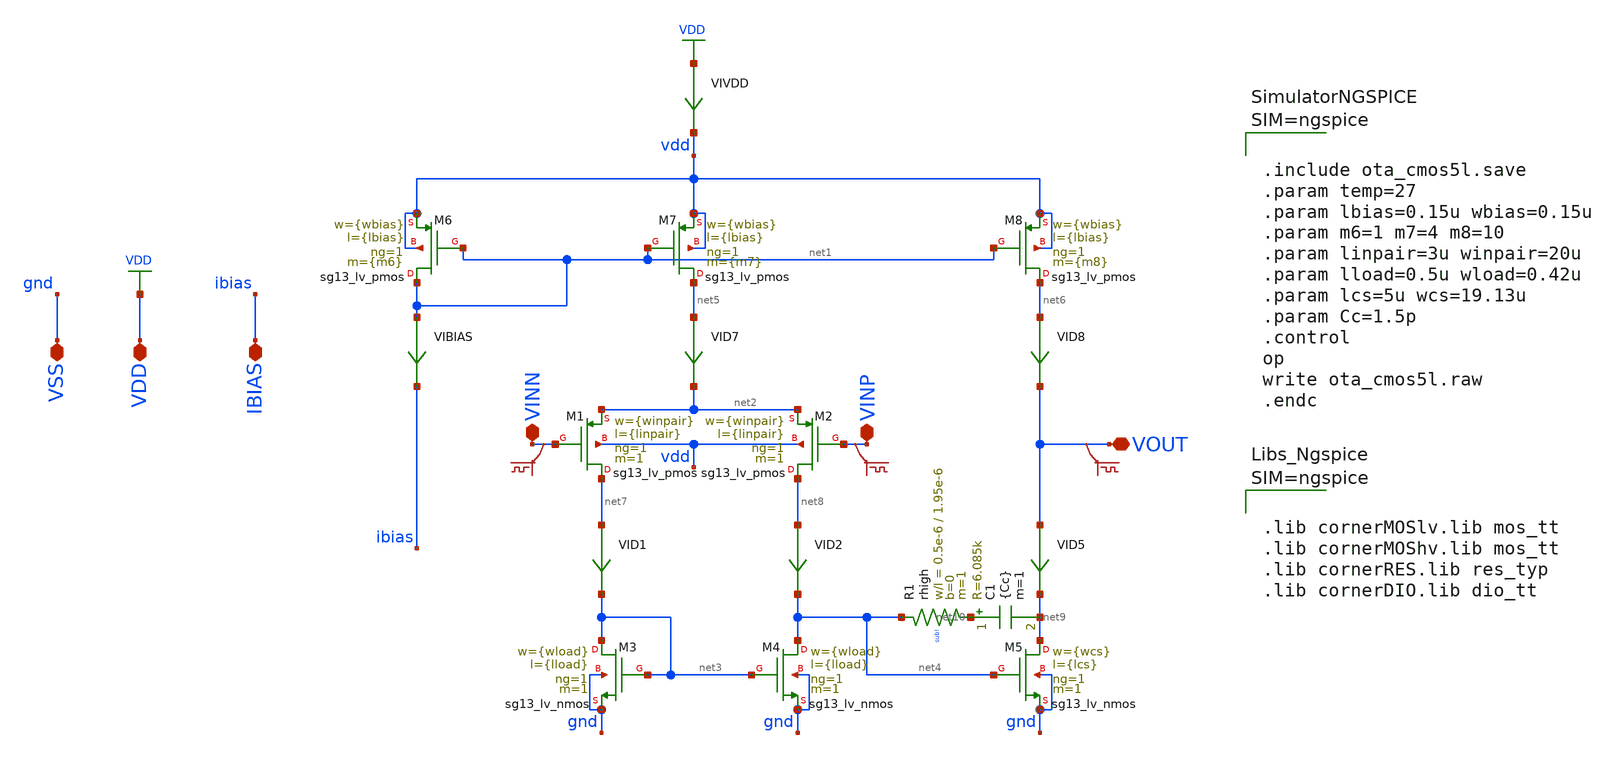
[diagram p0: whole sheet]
** sch_path: designs/libs/core_analog/ota_cmos5l/ota_cmos5l.sch
**.subckt ota_cmos5l IBIAS VDD VSS VOUT VINP VINN
*.iopin IBIAS
*.iopin VDD
*.iopin VSS
*.iopin VOUT
*.iopin VINP
*.iopin VINN
XM6 net1 net1 vdd vdd sg13_lv_pmos w={wbias} l={lbias} ng=1 m={m6} mm_ok=1
XM7 net5 net1 vdd vdd sg13_lv_pmos w={wbias} l={lbias} ng=1 m={m7} mm_ok=1
XM8 net6 net1 vdd vdd sg13_lv_pmos w={wbias} l={lbias} ng=1 m={m8} mm_ok=1
XM1 net7 VINN net2 vdd sg13_lv_pmos w={winpair} l={linpair} ng=1 m=1 mm_ok=1
XM2 net8 VINP net2 vdd sg13_lv_pmos w={winpair} l={linpair} ng=1 m=1 mm_ok=1
XM3 net3 net3 gnd gnd sg13_lv_nmos w={wload} l={lload} ng=1 m=1 mm_ok=1
XM4 net4 net3 gnd gnd sg13_lv_nmos w={wload} l={lload} ng=1 m=1 mm_ok=1
XM5 net9 net4 gnd gnd sg13_lv_nmos w={wcs} l={lcs} ng=1 m=1 mm_ok=1
C1 net10 net9 {Cc} m=1
XR1 net4 net10 sub! rhigh w=0.5e-6 l=1.95e-6 m=1 b=0 mm_ok=1
VIBIAS net1 ibias 0
.save i(vibias)
VID7 net5 net2 0
.save i(vid7)
VID8 net6 VOUT 0
.save i(vid8)
VIVDD VDD vdd 0
.save i(vivdd)
.save v(vinp)
.save v(vinn)
.save v(vout)
VID1 net7 net3 0
.save i(vid1)
VID2 net8 net4 0
.save i(vid2)
VID5 VOUT net9 0
.save i(vid5)
**** begin user architecture code



.include ota_cmos5l.save
.param temp=27
.param lbias=0.15u wbias=0.15u
.param m6=1 m7=4 m8=10
.param linpair=3u winpair=20u
.param lload=0.5u wload=0.42u
.param lcs=5u wcs=19.13u
.param Cc=1.5p
.control
op
write ota_cmos5l.raw
.endc






.lib cornerMOSlv.lib mos_tt
.lib cornerMOShv.lib mos_tt
.lib cornerRES.lib res_typ
.lib cornerDIO.lib dio_tt



**** end user architecture code
**.ends
.GLOBAL VDD
.end
